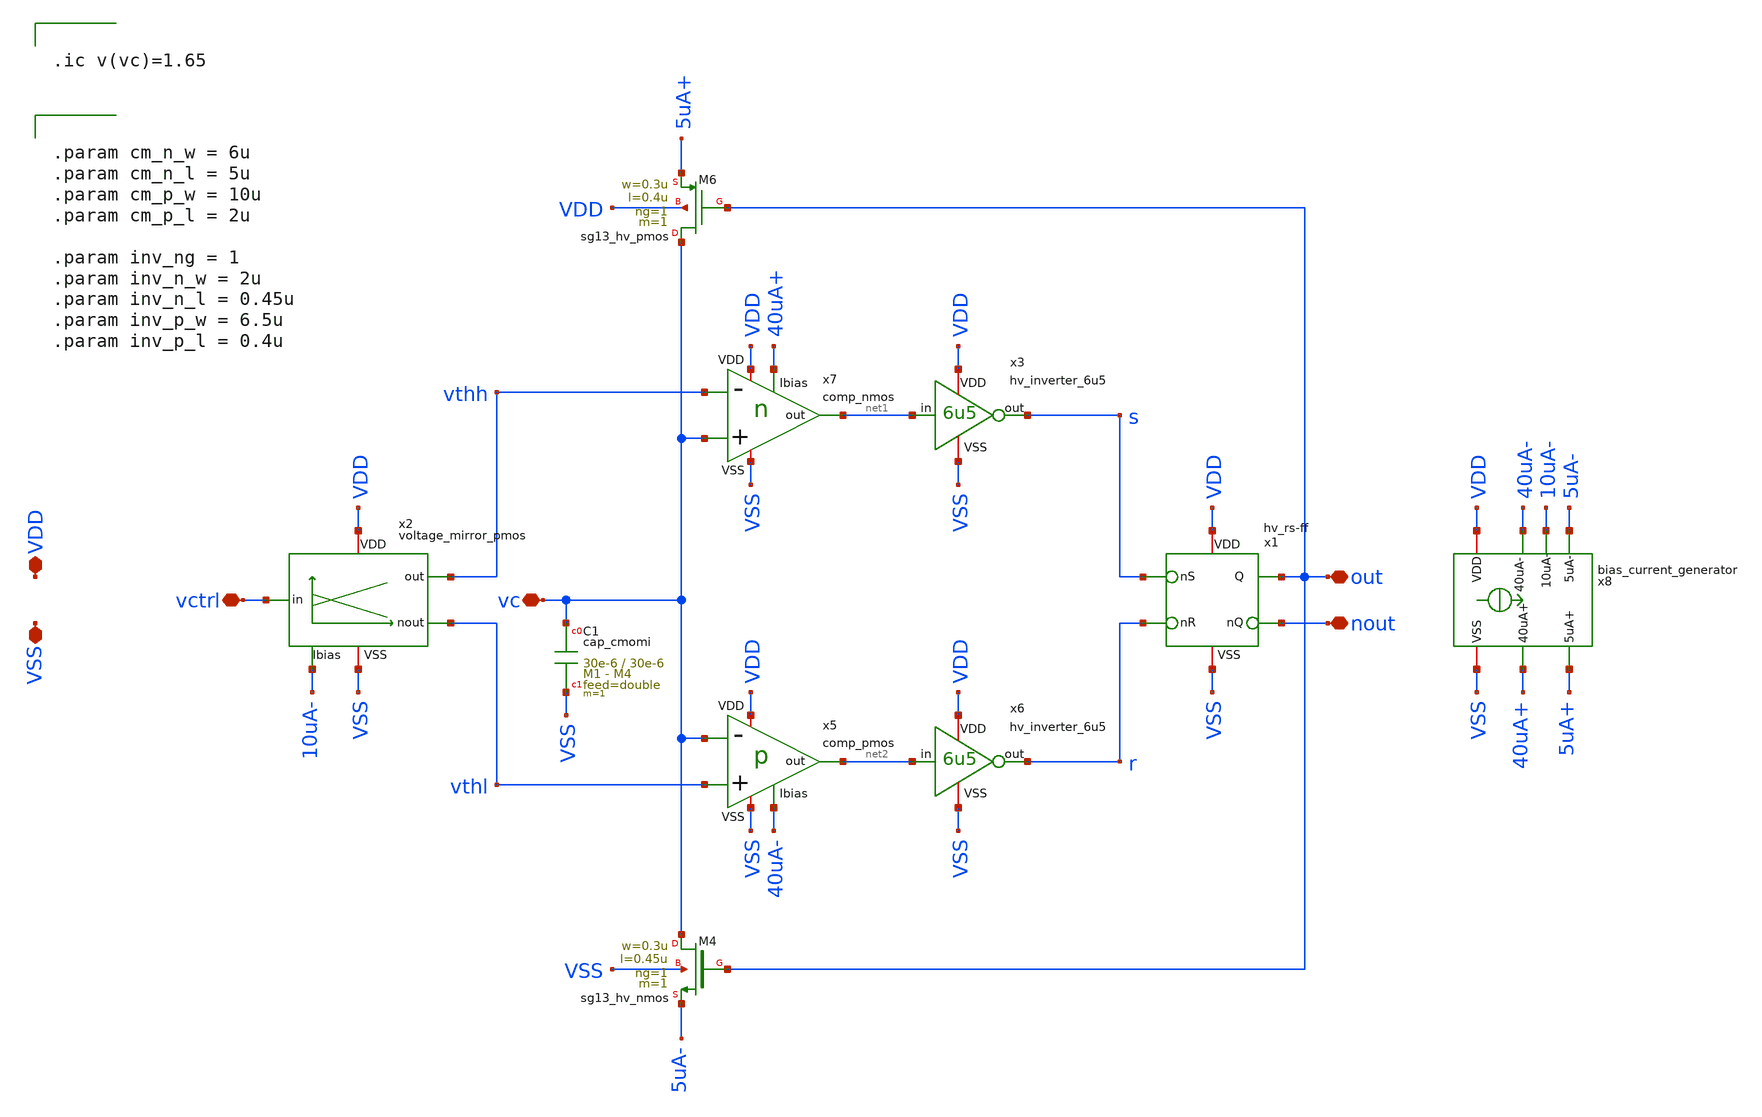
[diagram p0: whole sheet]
** sch_path: macros/heichips26_vcr/macros/switched_capacitor/schematic/xschem/vco.sch
**.subckt vco VSS VDD nout out vctrl vc
*.iopin VSS
*.iopin VDD
*.iopin nout
*.iopin out
*.iopin vctrl
*.iopin vc
XC1 vc VSS cap_cmomi w=30e-6 l=30e-6 mmin=1 mmax=4 feed=double subblock=0 m=1 mm_ok=1
XM4 vc out 5uA- VSS sg13_hv_nmos w=0.3u l=0.45u ng=1 m=1 mm_ok=1
x1 VDD s out nout r VSS hv_rs-ff
XM6 vc out 5uA+ VDD sg13_hv_pmos w=0.3u l=0.4u ng=1 m=1 mm_ok=1
x5 net2 vc vthl VDD 40uA- VSS comp_pmos
x7 net1 vthh vc VDD 40uA+ VSS comp_nmos
x2 10uA- vthl VDD vctrl VSS vthh voltage_mirror_pmos
x3 VDD net1 s VSS hv_inverter_6u5
x6 VDD net2 r VSS hv_inverter_6u5
x8 40uA+ 5uA+ VDD VSS 5uA- 10uA- 40uA- bias_current_generator
**** begin user architecture code


.ic v(vc)=1.65




.param cm_n_w = 6u
.param cm_n_l = 5u
.param cm_p_w = 10u
.param cm_p_l = 2u

.param inv_ng = 1
.param inv_n_w = 2u
.param inv_n_l = 0.45u
.param inv_p_w = 6.5u
.param inv_p_l = 0.4u


**** end user architecture code
**.ends

* expanding   symbol:  hv_rs-ff.sym # of pins=6
** sym_path: macros/heichips26_vcr/macros/switched_capacitor/schematic/xschem/hv_rs-ff.sym
** sch_path: macros/heichips26_vcr/macros/switched_capacitor/schematic/xschem/hv_rs-ff.sch
.subckt hv_rs-ff VDD nS Q nQ nR VSS
*.ipin nS
*.iopin VDD
*.iopin VSS
*.opin Q
*.ipin nR
*.opin nQ
x4 VDD nS Q nQ VSS hv_nand
x5 VDD Q nQ nR VSS hv_nand
.ends


* expanding   symbol:  comp_pmos.sym # of pins=6
** sym_path: macros/heichips26_vcr/macros/switched_capacitor/schematic/xschem/comp_pmos.sym
** sch_path: macros/heichips26_vcr/macros/switched_capacitor/schematic/xschem/comp_pmos.sch
.subckt comp_pmos out - + VDD Ibias VSS
*.iopin VDD
*.iopin VSS
*.ipin Ibias
*.opin out
*.ipin +
*.ipin -
**** begin user architecture code


.param n_w = 1.2u
.param n_l = 1.5u
.param p_w = 2u
.param p_l = 0.4u
.param bcm = 1


**** end user architecture code
XM9 net1 Ibias VDD VDD sg13_hv_pmos w=bcm*p_w l=p_l ng=1 m=1 mm_ok=1
XM10 out Ibias VDD VDD sg13_hv_pmos w=bcm*p_w l=p_l ng=1 m=1 mm_ok=1
XM11 Ibias Ibias VDD VDD sg13_hv_pmos w=p_w l=p_l ng=1 m=1 mm_ok=1
XM12 net3 + net1 VDD sg13_hv_pmos w=p_w l=p_l ng=1 m=1 mm_ok=1
XM13 net2 - net1 VDD sg13_hv_pmos w=p_w l=p_l ng=1 m=1 mm_ok=1
XM14 net3 net2 VSS VSS sg13_hv_nmos w=n_w l=n_l ng=1 m=1 mm_ok=1
XM15 net2 net2 VSS VSS sg13_hv_nmos w=n_w l=n_l ng=1 m=1 mm_ok=1
XM16 out net3 VSS VSS sg13_hv_nmos w=n_w l=n_l ng=1 m=1 mm_ok=1
.ends


* expanding   symbol:  comp_nmos.sym # of pins=6
** sym_path: macros/heichips26_vcr/macros/switched_capacitor/schematic/xschem/comp_nmos.sym
** sch_path: macros/heichips26_vcr/macros/switched_capacitor/schematic/xschem/comp_nmos.sch
.subckt comp_nmos out - + VDD Ibias VSS
*.iopin VDD
*.iopin VSS
*.ipin -
*.ipin +
*.ipin Ibias
*.opin out
XM8 net2 + net3 VSS sg13_hv_nmos w=n_w l=n_l ng=1 m=1 mm_ok=1
XM6 net1 net1 VDD VDD sg13_hv_pmos w=p_w l=p_l ng=1 m=1 mm_ok=1
XM1 net2 net1 VDD VDD sg13_hv_pmos w=p_w l=p_l ng=1 m=1 mm_ok=1
XM3 net1 - net3 VSS sg13_hv_nmos w=n_w l=n_l ng=1 m=1 mm_ok=1
**** begin user architecture code


.param n_w = 1.2u
.param n_l = 1.5u
.param p_w = 2u
.param p_l = 0.4u


**** end user architecture code
XM2 out net2 VDD VDD sg13_hv_pmos w=p_w l=p_l ng=1 m=1 mm_ok=1
XM4 net3 Ibias VSS VSS sg13_hv_nmos w=2*n_w l=n_l ng=1 m=1 mm_ok=1
XM5 out Ibias VSS VSS sg13_hv_nmos w=2*n_w l=n_l ng=1 m=1 mm_ok=1
XM7 Ibias Ibias VSS VSS sg13_hv_nmos w=n_w l=n_l ng=1 m=1 mm_ok=1
.ends


* expanding   symbol:  voltage_mirror_pmos.sym # of pins=6
** sym_path: macros/heichips26_vcr/macros/switched_capacitor/schematic/xschem/voltage_mirror_pmos.sym
** sch_path: macros/heichips26_vcr/macros/switched_capacitor/schematic/xschem/voltage_mirror_pmos.sch
.subckt voltage_mirror_pmos Ibias nout VDD in VSS out
*.iopin VDD
*.iopin VSS
*.ipin in
*.opin out
*.opin nout
*.ipin Ibias
**** begin user architecture code


.param n_w = 6u
.param n_l = 5u
.param p_w = 10u
.param p_l = 2u


**** end user architecture code
XR1 in Ibias VSS rhigh w=0.5e-6 l=34e-6 m=1 b=0 mm_ok=1
XM4 net1 Ibias VDD VDD sg13_hv_pmos w=p_w l=p_l ng=1 m=1 mm_ok=1
XM5 out net1 VSS VSS sg13_hv_nmos w=n_w l=n_l ng=1 m=1 mm_ok=1
XR2 VSS nout VSS rhigh w=0.5e-6 l=34e-6 m=1 b=0 mm_ok=1
XR3 out VDD VSS rhigh w=0.5e-6 l=34e-6 m=1 b=0 mm_ok=1
XM2 net1 net1 VSS VSS sg13_hv_nmos w=n_w l=n_l ng=1 m=1 mm_ok=1
XM3 nout Ibias VDD VDD sg13_hv_pmos w=p_w l=p_l ng=1 m=1 mm_ok=1
XM6 Ibias Ibias VDD VDD sg13_hv_pmos w=1.9*p_w l=p_l ng=1 m=1 mm_ok=1
.ends


* expanding   symbol:  hv_inverter_6u5.sym # of pins=4
** sym_path: macros/heichips26_vcr/macros/switched_capacitor/schematic/xschem/hv_inverter_6u5.sym
** sch_path: macros/heichips26_vcr/macros/switched_capacitor/schematic/xschem/hv_inverter_6u5.sch
.subckt hv_inverter_6u5 VDD in out VSS
*.ipin in
*.iopin VDD
*.iopin VSS
*.opin out
XM2 out in VSS VSS sg13_hv_nmos w={n_w} l={n_l} ng={ng} m=1 mm_ok=1
XM3 out in VDD VDD sg13_hv_pmos w={p_w} l={p_l} ng={ng} m=1 mm_ok=1
**** begin user architecture code


.param ng  = 1
.param n_ng = ng
.param n_w = {2u*n_ng}
.param n_l = 0.45u
.param p_ng = ng
.param p_w = {6.5u*p_ng}
.param p_l = 0.4u


**** end user architecture code
.ends


* expanding   symbol:  bias_current_generator.sym # of pins=7
** sym_path: macros/heichips26_vcr/macros/switched_capacitor/schematic/xschem/bias_current_generator.sym
** sch_path: macros/heichips26_vcr/macros/switched_capacitor/schematic/xschem/bias_current_generator.sch
.subckt bias_current_generator 40uA+ 5uA+ VDD VSS 5uA- 10uA- 40uA-
*.opin 40uA+
*.iopin VSS
*.iopin VDD
*.opin 40uA-
*.opin 10uA-
*.opin 5uA+
*.opin 5uA-
x4 VDD net1 VSS current_reference_40uA
XM11 net1 net1 VDD VDD sg13_hv_pmos w=cm_p_w l=cm_p_l ng=1 m=1 mm_ok=1
XM12 40uA+ net1 VDD VDD sg13_hv_pmos w=cm_p_w l=cm_p_l ng=1 m=1 mm_ok=1
XM13 net2 net1 VDD VDD sg13_hv_pmos w=cm_p_w l=cm_p_l ng=1 m=1 mm_ok=1
XM14 net2 net2 VSS VSS sg13_hv_nmos w=cm_n_w l=cm_n_l ng=1 m=1 mm_ok=1
XM15 40uA- net2 VSS VSS sg13_hv_nmos w=cm_n_w l=cm_n_l ng=1 m=1 mm_ok=1
XM1 net3 net1 VDD VDD sg13_hv_pmos w=cm_p_w l=cm_p_l ng=1 m=1 mm_ok=1
XM2 net3 net3 VSS VSS sg13_hv_nmos w=4*cm_n_w l=cm_n_l ng=4 m=1 mm_ok=1
XM3 10uA- net3 VSS VSS sg13_hv_nmos w=cm_n_w l=cm_n_l ng=1 m=1 mm_ok=1
XM5 net4 net3 VSS VSS sg13_hv_nmos w=cm_n_w l=cm_n_l ng=1 m=1 mm_ok=1
XM25 net4 net4 VDD VDD sg13_hv_pmos w=2*cm_p_w l=cm_p_l ng=2 m=1 mm_ok=1
XM26 net5 net4 VDD VDD sg13_hv_pmos w=cm_p_w l=cm_p_l ng=1 m=1 mm_ok=1
XM27 5uA+ net4 VDD VDD sg13_hv_pmos w=cm_p_w l=cm_p_l ng=1 m=1 mm_ok=1
XM28 net5 net5 VSS VSS sg13_hv_nmos w=cm_n_w l=cm_n_l ng=2 m=1 mm_ok=1
XM29 5uA- net5 VSS VSS sg13_hv_nmos w=cm_n_w l=cm_n_l ng=1 m=1 mm_ok=1
**** begin user architecture code


.param cm_n_w = 6u
.param cm_n_l = 5u
.param cm_p_w = 10u
.param cm_p_l = 2u


**** end user architecture code
.ends


* expanding   symbol:  hv_nand.sym # of pins=5
** sym_path: macros/heichips26_vcr/macros/switched_capacitor/schematic/xschem/hv_nand.sym
** sch_path: macros/heichips26_vcr/macros/switched_capacitor/schematic/xschem/hv_nand.sch
.subckt hv_nand VDD in1 out in2 VSS
*.ipin in1
*.iopin VDD
*.iopin VSS
*.opin out
*.ipin in2
**** begin user architecture code


.param w   = 10u
.param ng  = 4
.param n_ng = ng
.param n_w = {3u*n_ng}
.param n_l = 0.45u
.param p_ng = ng
.param p_w = {10u*p_ng}
.param p_l = 0.4u


**** end user architecture code
XM2 out in1 net1 VSS sg13_hv_nmos w={n_w} l={n_l} ng={ng} m=1 mm_ok=1
XM3 out in2 VDD VDD sg13_hv_pmos w={p_w} l={p_l} ng={ng} m=1 mm_ok=1
XM1 net1 in2 VSS VSS sg13_hv_nmos w={n_w} l={n_l} ng={ng} m=1 mm_ok=1
XM4 out in1 VDD VDD sg13_hv_pmos w={p_w} l={p_l} ng={ng} m=1 mm_ok=1
.ends


* expanding   symbol:  current_reference_40uA.sym # of pins=3
** sym_path: macros/heichips26_vcr/macros/switched_capacitor/schematic/xschem/current_reference_40uA.sym
** sch_path: macros/heichips26_vcr/macros/switched_capacitor/schematic/xschem/current_reference_40uA.sch
.subckt current_reference_40uA VDD iout VSS
*.iopin VSS
*.iopin VDD
*.iopin iout
XM8 net2 net2 VSS VSS sg13_hv_nmos w=n_w l=n_l ng=1 m=1 mm_ok=1
XM6 net2 net1 VDD VDD sg13_hv_pmos w=p_w l=p_l ng=1 m=1 mm_ok=1
XM1 net1 net1 VDD VDD sg13_hv_pmos w=p_w l=p_l ng=1 m=1 mm_ok=1
XM3 net1 net2 net3 VSS sg13_hv_nmos w=n_w l=n_l ng=1 m=1 mm_ok=1
XR2 net4 VSS VSS rppd w=2e-6 l=21.9e-6 m=1 b=0 mm_ok=1
XM2 net1 net2 net3 VSS sg13_hv_nmos w=n_w l=n_l ng=1 m=1 mm_ok=1
XM4 net1 net2 net3 VSS sg13_hv_nmos w=n_w l=n_l ng=1 m=1 mm_ok=1
XM5 net1 net2 net3 VSS sg13_hv_nmos w=n_w l=n_l ng=1 m=1 mm_ok=1
XM7 iout net2 VSS VSS sg13_hv_nmos w=n_w l=n_l ng=1 m=1 mm_ok=1
XR3 net3 net4 VSS rsil w=0.5e-6 l=365e-6 m=1 mm_ok=1
**** begin user architecture code


.param n_w = 6u
.param n_l = 5u
.param p_w = 10u
.param p_l = 2u


**** end user architecture code
.ends

.end
